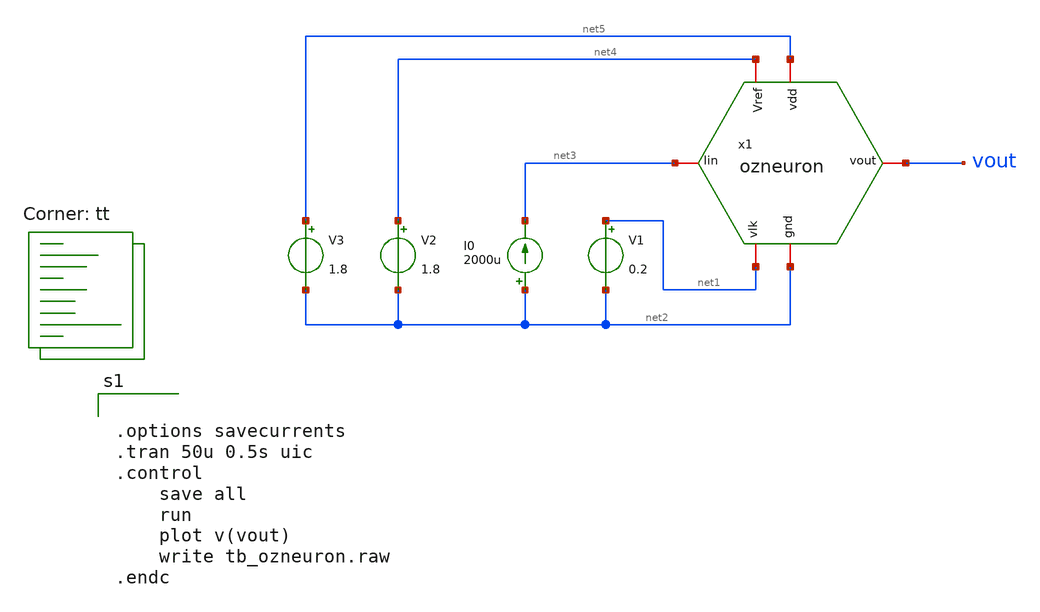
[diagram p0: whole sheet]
** sch_path: Neuron/OZNeuron/tb_ozneuron.sch
**.subckt tb_ozneuron
x1 net5 net3 vout net1 net4 net2 ozneuron
V1 net1 net2 0.2
V2 net4 net2 1.8
V3 net5 net2 1.8
I0 net2 net3 2000u
**** begin user architecture code
.lib $::SKYWATER_MODELS/sky130.lib.spice tt


.options savecurrents
.tran 50u 0.5s uic
.control
	save all
	run
	plot v(vout)
	write tb_ozneuron.raw
.endc


**** end user architecture code
**.ends

* expanding   symbol:  /home/alex/Desktop/EDA/SNN_IPN/Neuron/OZNeuron/ozneuron.sym # of pins=6
** sym_path: Neuron/OZNeuron/ozneuron.sym
** sch_path: Neuron/OZNeuron/ozneuron.sch
.subckt ozneuron vdd Iin vout vlk Vref gnd
*.iopin Vref
*.iopin gnd
*.iopin vdd
*.iopin vlk
*.iopin vout
*.iopin Iin
XMna Iin va vdd vdd sky130_fd_pr__pfet_01v8 L=0.15 W=2 nf=1 ad='int((nf+1)/2) * W/nf * 0.29' as='int((nf+2)/2) * W/nf * 0.29'
+ pd='2*int((nf+1)/2) * (W/nf + 0.29)' ps='2*int((nf+2)/2) * (W/nf + 0.29)' nrd='0.29 / W' nrs='0.29 / W'
+ sa=0 sb=0 sd=0 mult=1 m=1
XMlk Iin vlk gnd gnd sky130_fd_pr__nfet_01v8 L=0.15 W=1 nf=1 ad='int((1 + 1)/2) * 1 / 1 * 0.29' as='int((1 + 2)/2) * 1 / 1 * 0.29'
+ pd='2*int((1 + 1)/2) * (1 / 1 + 0.29)' ps='2*int((1 + 2)/2) * (1 / 1 + 0.29)' nrd='0.29 / 1 ' nrs='0.29 / 1 '
+ sa=0 sb=0 sd=0 mult=1 m=1
XMinv1 va Iin vdd vdd sky130_fd_pr__pfet_01v8 L=0.15 W=2 nf=1 ad='int((nf+1)/2) * W/nf * 0.29' as='int((nf+2)/2) * W/nf * 0.29'
+ pd='2*int((nf+1)/2) * (W/nf + 0.29)' ps='2*int((nf+2)/2) * (W/nf + 0.29)' nrd='0.29 / W' nrs='0.29 / W'
+ sa=0 sb=0 sd=0 mult=1 m=1
XMinv2 vout va vdd vdd sky130_fd_pr__pfet_01v8 L=0.15 W=2 nf=1 ad='int((nf+1)/2) * W/nf * 0.29' as='int((nf+2)/2) * W/nf * 0.29'
+ pd='2*int((nf+1)/2) * (W/nf + 0.29)' ps='2*int((nf+2)/2) * (W/nf + 0.29)' nrd='0.29 / W' nrs='0.29 / W'
+ sa=0 sb=0 sd=0 mult=1 m=1
XMref Iin vout gnd gnd sky130_fd_pr__nfet_01v8 L=0.15 W=1 nf=1 ad='int((1 + 1)/2) * 1 / 1 * 0.29' as='int((1 + 2)/2) * 1 / 1 * 0.29'
+ pd='2*int((1 + 1)/2) * (1 / 1 + 0.29)' ps='2*int((1 + 2)/2) * (1 / 1 + 0.29)' nrd='0.29 / 1 ' nrs='0.29 / 1 '
+ sa=0 sb=0 sd=0 mult=1 m=1
XMinv3 va Iin gnd gnd sky130_fd_pr__nfet_01v8 L=0.15 W=1 nf=1 ad='int((1 + 1)/2) * 1 / 1 * 0.29' as='int((1 + 2)/2) * 1 / 1 * 0.29'
+ pd='2*int((1 + 1)/2) * (1 / 1 + 0.29)' ps='2*int((1 + 2)/2) * (1 / 1 + 0.29)' nrd='0.29 / 1 ' nrs='0.29 / 1 '
+ sa=0 sb=0 sd=0 mult=1 m=1
XMinv4 vout va net1 gnd sky130_fd_pr__nfet_01v8 L=0.15 W=1 nf=1 ad='int((1 + 1)/2) * 1 / 1 * 0.29' as='int((1 + 2)/2) * 1 / 1 * 0.29'
+ pd='2*int((1 + 1)/2) * (1 / 1 + 0.29)' ps='2*int((1 + 2)/2) * (1 / 1 + 0.29)' nrd='0.29 / 1 ' nrs='0.29 / 1 '
+ sa=0 sb=0 sd=0 mult=1 m=1
XMref2 net1 Vref gnd gnd sky130_fd_pr__nfet_01v8 L=0.15 W=1 nf=1 ad='int((1 + 1)/2) * 1 / 1 * 0.29' as='int((1 + 2)/2) * 1 / 1 * 0.29'
+ pd='2*int((1 + 1)/2) * (1 / 1 + 0.29)' ps='2*int((1 + 2)/2) * (1 / 1 + 0.29)' nrd='0.29 / 1 ' nrs='0.29 / 1 '
+ sa=0 sb=0 sd=0 mult=1 m=1
Cmem Iin gnd 1p m=1
Ck vout gnd 1p m=1
.ends

.end
